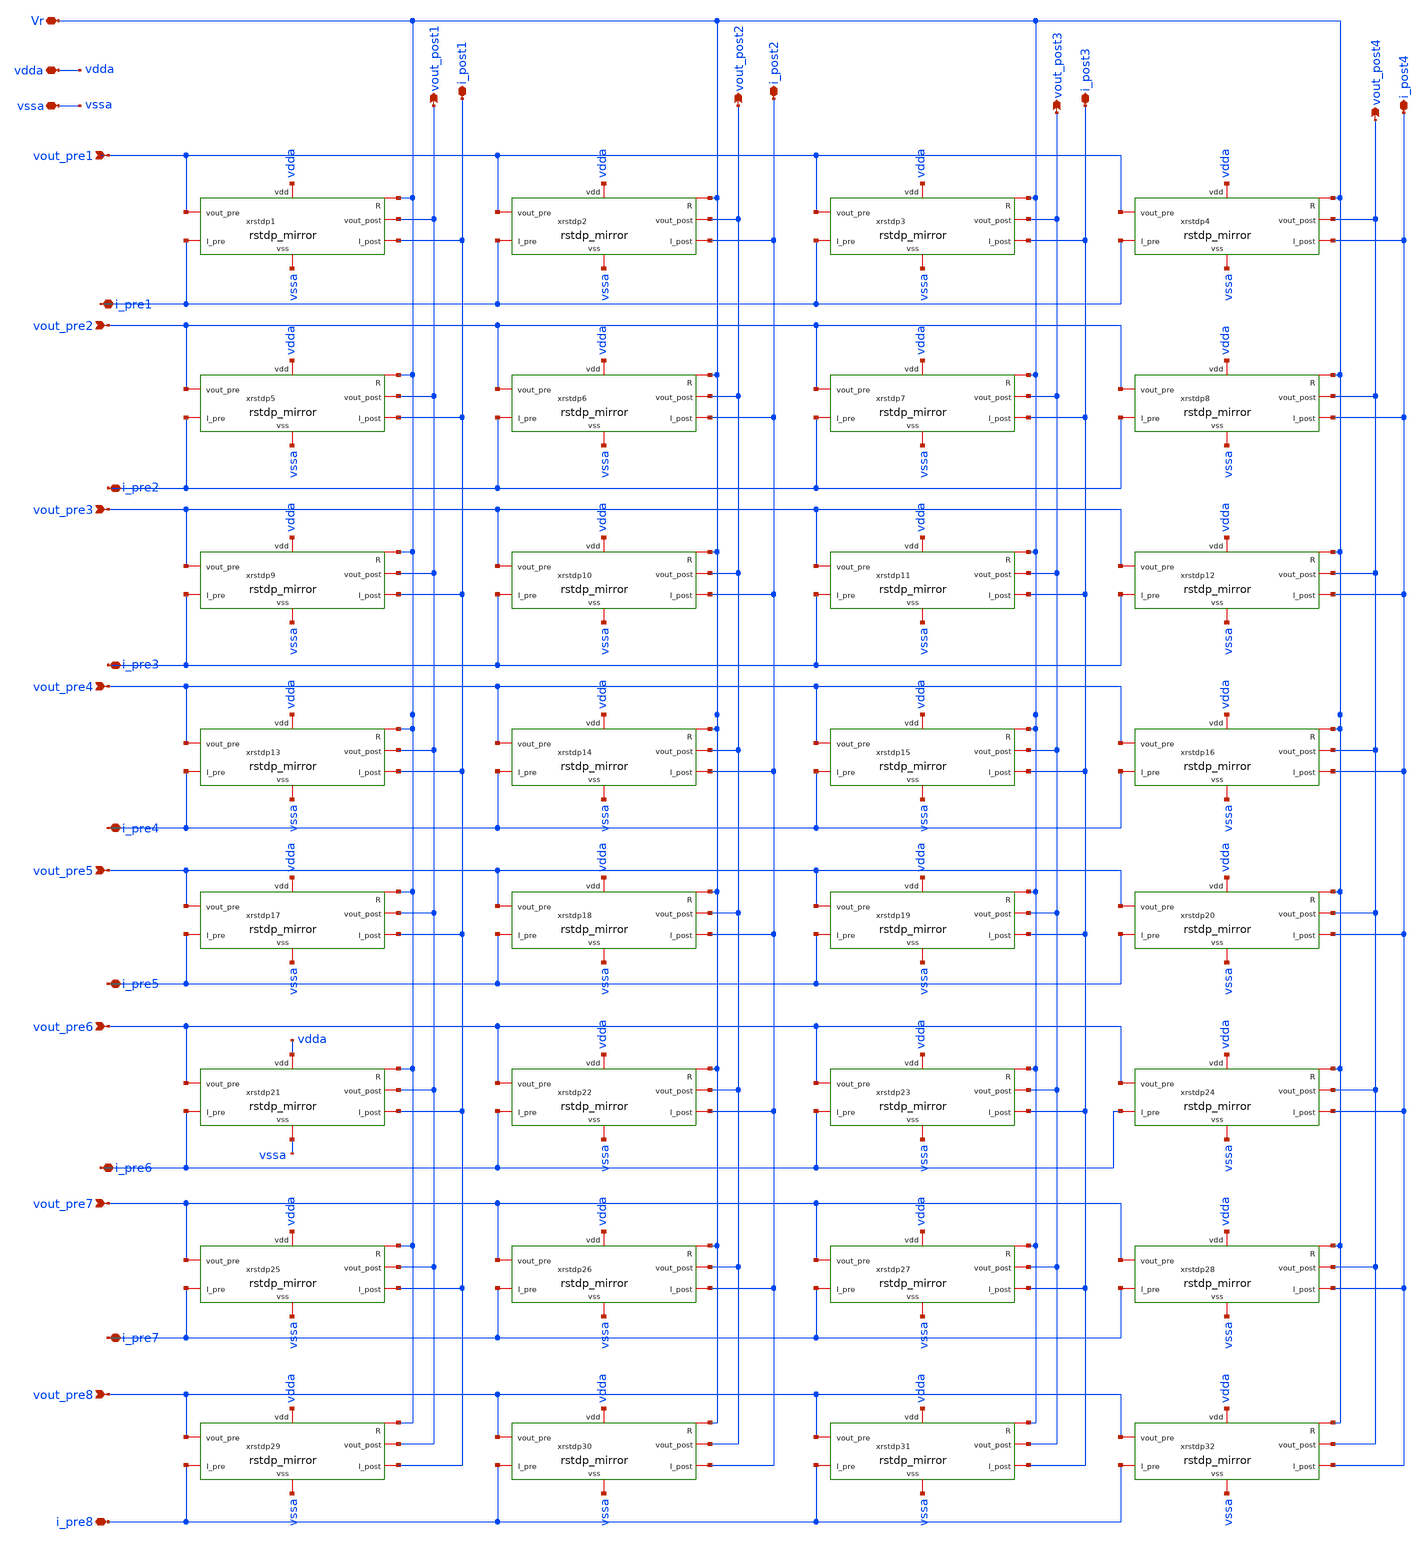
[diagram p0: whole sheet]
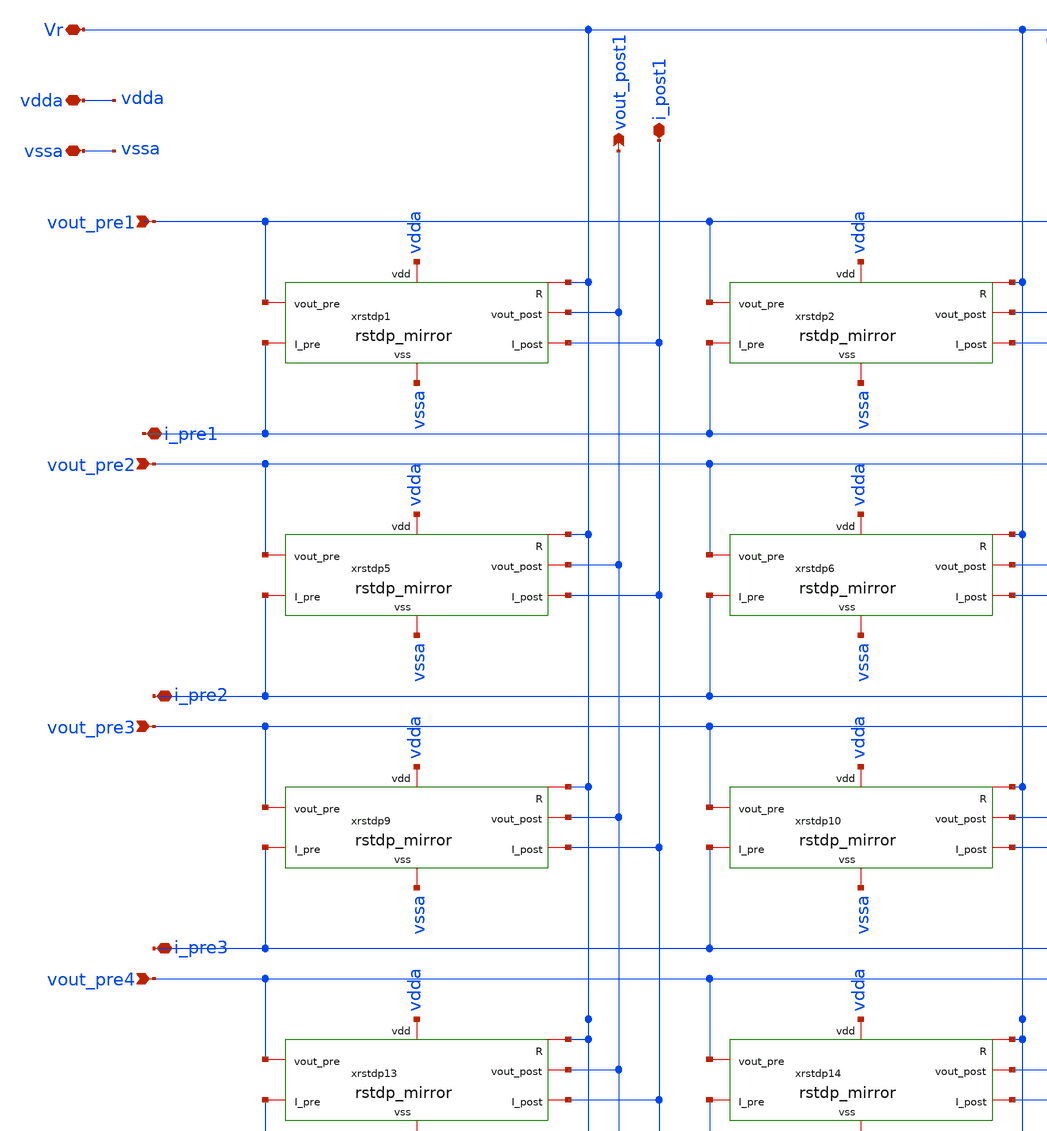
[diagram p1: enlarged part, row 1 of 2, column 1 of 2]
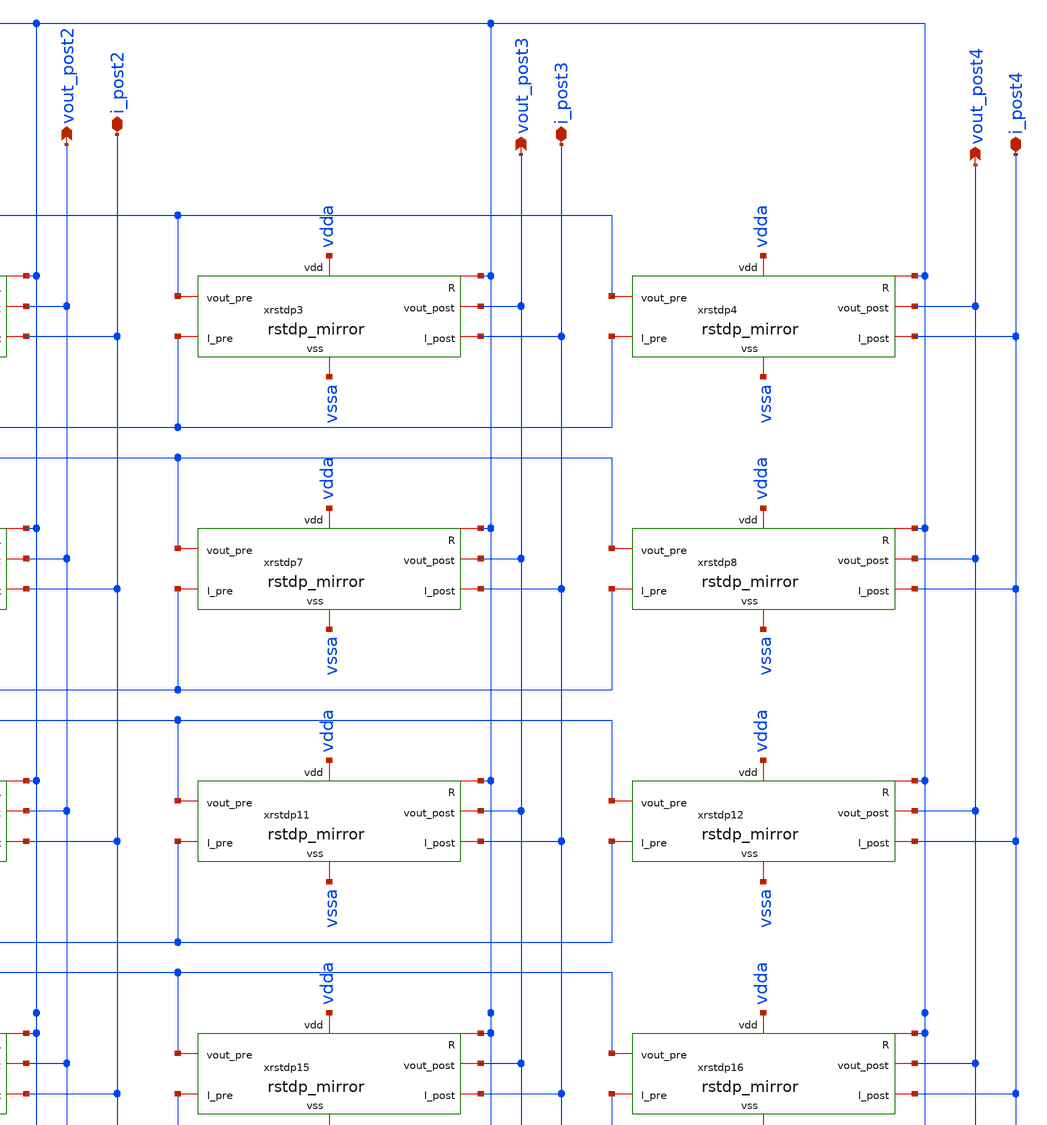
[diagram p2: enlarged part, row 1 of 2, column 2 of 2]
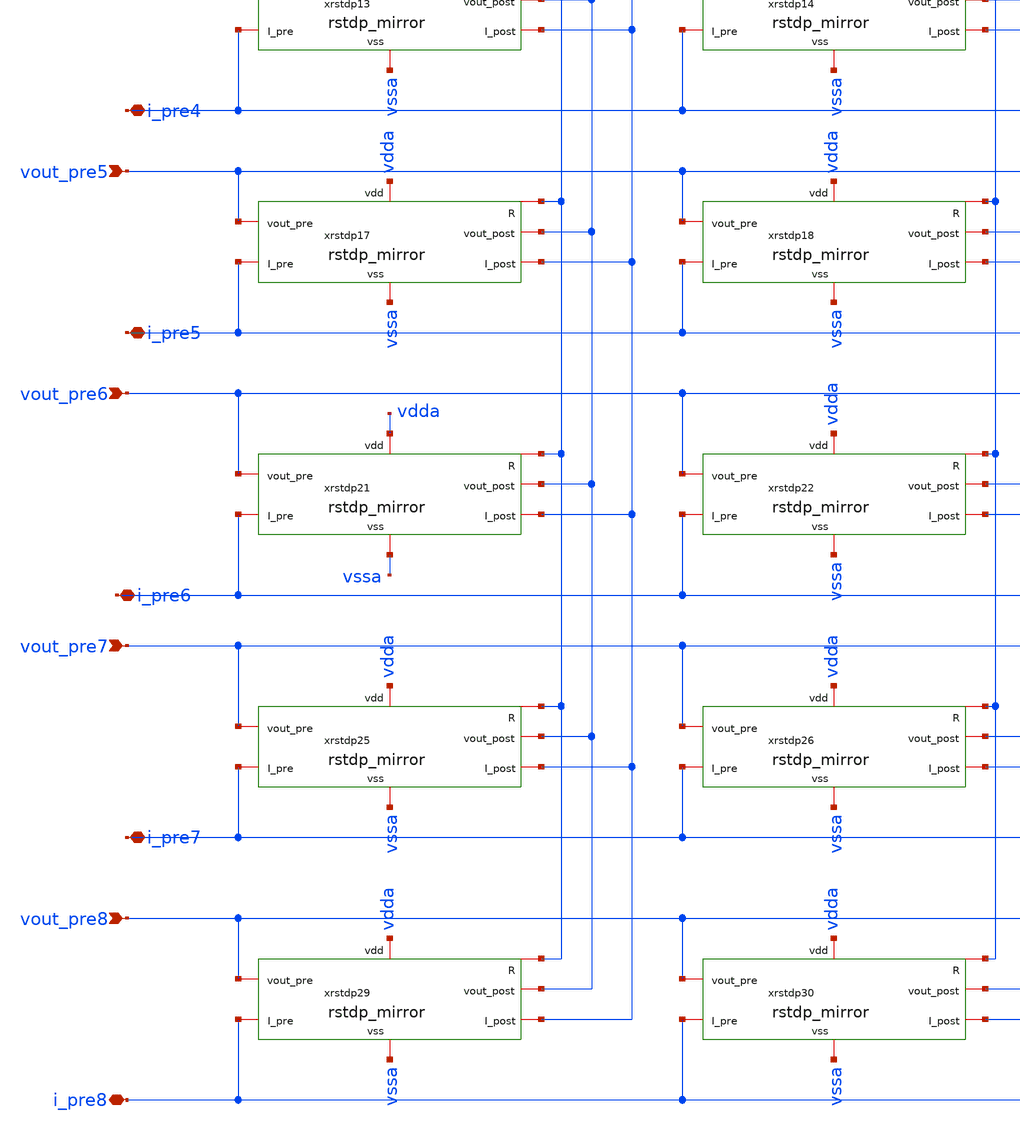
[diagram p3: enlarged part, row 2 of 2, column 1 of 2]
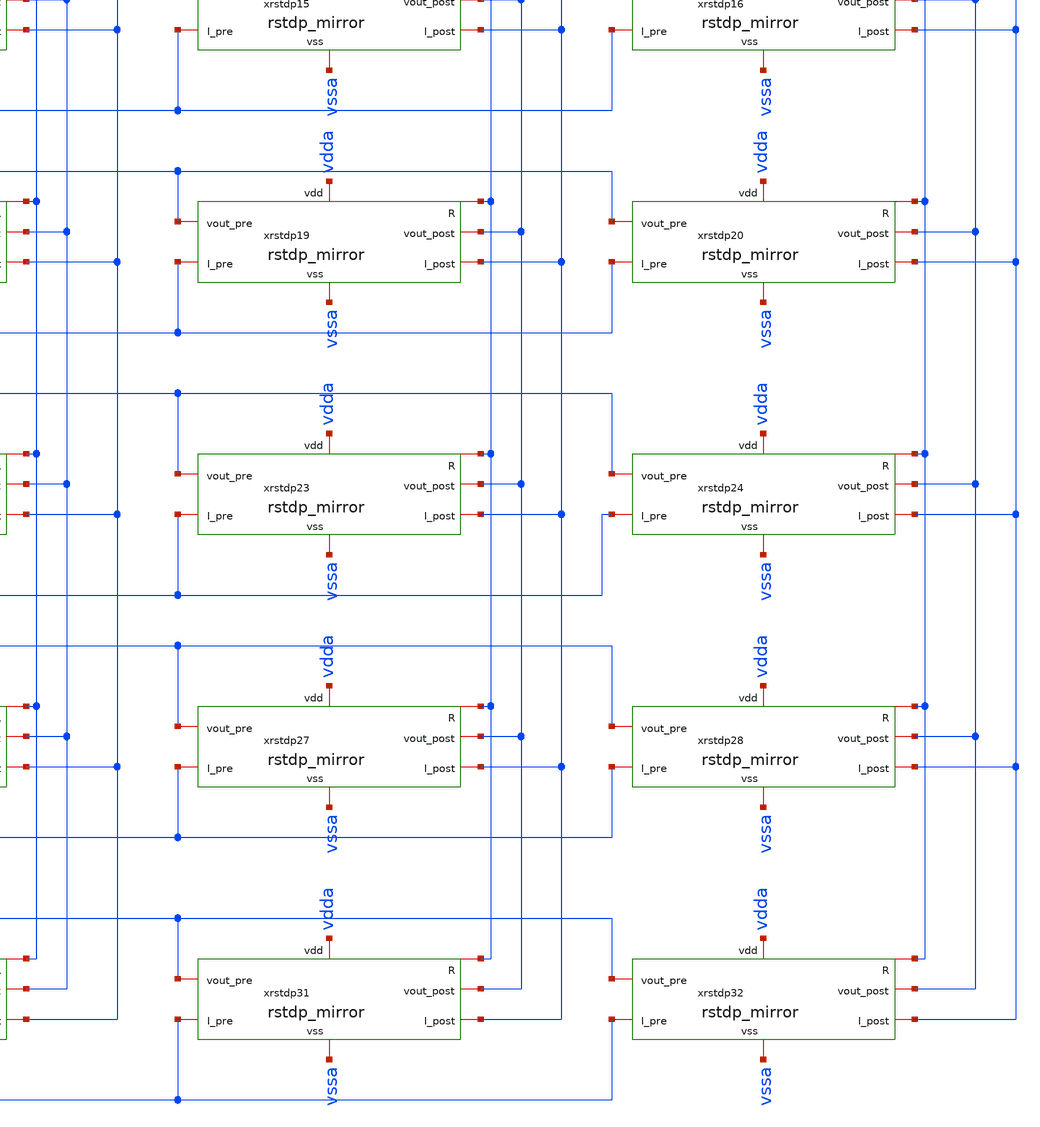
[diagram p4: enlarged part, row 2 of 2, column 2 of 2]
** sch_path: Synapse/rstdp_array_8x4.sch
**.subckt rstdp_array_8x4 vout_pre1 vout_post1 i_pre1 vdda vssa i_post1 i_post3 i_post4 i_pre2
*+ i_pre3 i_pre4 vout_pre2 vout_pre3 vout_pre4 vout_post2 vout_post3 vout_post4 i_post2 Vr i_pre5 i_pre6
*+ i_pre7 i_pre8 vout_pre5 vout_pre6 vout_pre7 vout_pre8
*.ipin vout_pre1
*.opin vout_post1
*.iopin i_pre1
*.iopin vdda
*.iopin vssa
*.iopin i_post1
*.iopin i_post3
*.iopin i_post4
*.iopin i_pre2
*.iopin i_pre3
*.iopin i_pre4
*.ipin vout_pre2
*.ipin vout_pre3
*.ipin vout_pre4
*.opin vout_post2
*.opin vout_post3
*.opin vout_post4
*.iopin i_post2
*.iopin Vr
*.iopin i_pre5
*.iopin i_pre6
*.iopin i_pre7
*.iopin i_pre8
*.ipin vout_pre5
*.ipin vout_pre6
*.ipin vout_pre7
*.ipin vout_pre8
xrstdp1 vdda Vr vssa vout_pre1 vout_post1 i_post1 i_pre1 rstdp_mirror
xrstdp2 vdda Vr vssa vout_pre1 vout_post2 i_post2 i_pre1 rstdp_mirror
xrstdp3 vdda Vr vssa vout_pre1 vout_post3 i_post3 i_pre1 rstdp_mirror
xrstdp4 vdda Vr vssa vout_pre1 vout_post4 i_post4 i_pre1 rstdp_mirror
xrstdp5 vdda Vr vssa vout_pre2 vout_post1 i_post1 i_pre2 rstdp_mirror
xrstdp6 vdda Vr vssa vout_pre2 vout_post2 i_post2 i_pre2 rstdp_mirror
xrstdp7 vdda Vr vssa vout_pre2 vout_post3 i_post3 i_pre2 rstdp_mirror
xrstdp8 vdda Vr vssa vout_pre2 vout_post4 i_post4 i_pre2 rstdp_mirror
xrstdp9 vdda Vr vssa vout_pre3 vout_post1 i_post1 i_pre3 rstdp_mirror
xrstdp10 vdda Vr vssa vout_pre3 vout_post2 i_post2 i_pre3 rstdp_mirror
xrstdp11 vdda Vr vssa vout_pre3 vout_post3 i_post3 i_pre3 rstdp_mirror
xrstdp12 vdda Vr vssa vout_pre3 vout_post4 i_post4 i_pre3 rstdp_mirror
xrstdp13 vdda Vr vssa vout_pre4 vout_post1 i_post1 i_pre4 rstdp_mirror
xrstdp14 vdda Vr vssa vout_pre4 vout_post2 i_post2 i_pre4 rstdp_mirror
xrstdp15 vdda Vr vssa vout_pre4 vout_post3 i_post3 i_pre4 rstdp_mirror
xrstdp16 vdda Vr vssa vout_pre4 vout_post4 i_post4 i_pre4 rstdp_mirror
xrstdp17 vdda Vr vssa vout_pre5 vout_post1 i_post1 i_pre5 rstdp_mirror
xrstdp18 vdda Vr vssa vout_pre5 vout_post2 i_post2 i_pre5 rstdp_mirror
xrstdp19 vdda Vr vssa vout_pre5 vout_post3 i_post3 i_pre5 rstdp_mirror
xrstdp20 vdda Vr vssa vout_pre5 vout_post4 i_post4 i_pre5 rstdp_mirror
xrstdp21 vdda Vr vssa vout_pre6 vout_post1 i_post1 i_pre6 rstdp_mirror
xrstdp22 vdda Vr vssa vout_pre6 vout_post2 i_post2 i_pre6 rstdp_mirror
xrstdp23 vdda Vr vssa vout_pre6 vout_post3 i_post3 i_pre6 rstdp_mirror
xrstdp24 vdda Vr vssa vout_pre6 vout_post4 i_post4 i_pre6 rstdp_mirror
xrstdp25 vdda Vr vssa vout_pre7 vout_post1 i_post1 i_pre7 rstdp_mirror
xrstdp26 vdda Vr vssa vout_pre7 vout_post2 i_post2 i_pre7 rstdp_mirror
xrstdp27 vdda Vr vssa vout_pre7 vout_post3 i_post3 i_pre7 rstdp_mirror
xrstdp28 vdda Vr vssa vout_pre7 vout_post4 i_post4 i_pre7 rstdp_mirror
xrstdp29 vdda Vr vssa vout_pre8 vout_post1 i_post1 i_pre8 rstdp_mirror
xrstdp30 vdda Vr vssa vout_pre8 vout_post2 i_post2 i_pre8 rstdp_mirror
xrstdp31 vdda Vr vssa vout_pre8 vout_post3 i_post3 i_pre8 rstdp_mirror
xrstdp32 vdda Vr vssa vout_pre8 vout_post4 i_post4 i_pre8 rstdp_mirror
**.ends

* expanding   symbol:  Synapse/rstdp_mirror.sym # of pins=7
** sym_path: Synapse/rstdp_mirror.sym
** sch_path: Synapse/rstdp_mirror.sch
.subckt rstdp_mirror vdd R vss vout_pre vout_post I_post I_pre
*.iopin vdd
*.iopin vss
*.iopin R
*.iopin vout_post
*.iopin vout_pre
*.iopin I_post
*.iopin I_pre
XM2 A vout_pre vpre vss sky130_fd_pr__nfet_01v8 L=0.15 W=1.5 nf=1 ad='int((nf+1)/2) * W/nf * 0.29' as='int((nf+2)/2) * W/nf * 0.29'
+ pd='2*int((nf+1)/2) * (W/nf + 0.29)' ps='2*int((nf+2)/2) * (W/nf + 0.29)' nrd='0.29 / W' nrs='0.29 / W'
+ sa=0 sb=0 sd=0 mult=1 m=1
XM3 vpre vout_post vss vss sky130_fd_pr__nfet_01v8 L=0.15 W=1.5 nf=1 ad='int((nf+1)/2) * W/nf * 0.29'
+ as='int((nf+2)/2) * W/nf * 0.29' pd='2*int((nf+1)/2) * (W/nf + 0.29)' ps='2*int((nf+2)/2) * (W/nf + 0.29)'
+ nrd='0.29 / W' nrs='0.29 / W' sa=0 sb=0 sd=0 mult=1 m=1
XM1 A vout_post vpost vss sky130_fd_pr__nfet_01v8 L=0.15 W=1.5 nf=1 ad='int((nf+1)/2) * W/nf * 0.29'
+ as='int((nf+2)/2) * W/nf * 0.29' pd='2*int((nf+1)/2) * (W/nf + 0.29)' ps='2*int((nf+2)/2) * (W/nf + 0.29)'
+ nrd='0.29 / W' nrs='0.29 / W' sa=0 sb=0 sd=0 mult=1 m=1
XM4 vpost vout_pre vss vss sky130_fd_pr__nfet_01v8 L=0.15 W=1.5 nf=1 ad='int((nf+1)/2) * W/nf * 0.29'
+ as='int((nf+2)/2) * W/nf * 0.29' pd='2*int((nf+1)/2) * (W/nf + 0.29)' ps='2*int((nf+2)/2) * (W/nf + 0.29)'
+ nrd='0.29 / W' nrs='0.29 / W' sa=0 sb=0 sd=0 mult=1 m=1
XM10 vss A vdd vdd sky130_fd_pr__pfet_01v8 L=5 W=0.5 nf=1 ad='int((nf+1)/2) * W/nf * 0.29' as='int((nf+2)/2) * W/nf * 0.29'
+ pd='2*int((nf+1)/2) * (W/nf + 0.29)' ps='2*int((nf+2)/2) * (W/nf + 0.29)' nrd='0.29 / W' nrs='0.29 / W'
+ sa=0 sb=0 sd=0 mult=1 m=1
XR2 te be rram_v0
XM5 vpre R be vss sky130_fd_pr__nfet_01v8 L=0.15 W=1.5 nf=1 ad='int((nf+1)/2) * W/nf * 0.29' as='int((nf+2)/2) * W/nf * 0.29'
+ pd='2*int((nf+1)/2) * (W/nf + 0.29)' ps='2*int((nf+2)/2) * (W/nf + 0.29)' nrd='0.29 / W' nrs='0.29 / W'
+ sa=0 sb=0 sd=0 mult=1 m=1
XM6 te R vpost vss sky130_fd_pr__nfet_01v8 L=0.15 W=1.5 nf=1 ad='int((nf+1)/2) * W/nf * 0.29' as='int((nf+2)/2) * W/nf * 0.29'
+ pd='2*int((nf+1)/2) * (W/nf + 0.29)' ps='2*int((nf+2)/2) * (W/nf + 0.29)' nrd='0.29 / W' nrs='0.29 / W'
+ sa=0 sb=0 sd=0 mult=1 m=1
XM7 vpre R te vdd sky130_fd_pr__pfet_01v8 L=0.15 W=3 nf=1 ad='int((nf+1)/2) * W/nf * 0.29' as='int((nf+2)/2) * W/nf * 0.29'
+ pd='2*int((nf+1)/2) * (W/nf + 0.29)' ps='2*int((nf+2)/2) * (W/nf + 0.29)' nrd='0.29 / W' nrs='0.29 / W'
+ sa=0 sb=0 sd=0 mult=1 m=1
XM8 be R vpost vdd sky130_fd_pr__pfet_01v8 L=0.15 W=3 nf=1 ad='int((nf+1)/2) * W/nf * 0.29' as='int((nf+2)/2) * W/nf * 0.29'
+ pd='2*int((nf+1)/2) * (W/nf + 0.29)' ps='2*int((nf+2)/2) * (W/nf + 0.29)' nrd='0.29 / W' nrs='0.29 / W'
+ sa=0 sb=0 sd=0 mult=1 m=1
XM14 I_post A vdd vdd sky130_fd_pr__pfet_01v8 L=0.4 W=1 nf=1 ad='int((nf+1)/2) * W/nf * 0.29' as='int((nf+2)/2) * W/nf * 0.29'
+ pd='2*int((nf+1)/2) * (W/nf + 0.29)' ps='2*int((nf+2)/2) * (W/nf + 0.29)' nrd='0.29 / W' nrs='0.29 / W'
+ sa=0 sb=0 sd=0 mult=1 m=1
XM15 A A vdd vdd sky130_fd_pr__pfet_01v8 L=0.15 W=2.5 nf=1 ad='int((nf+1)/2) * W/nf * 0.29' as='int((nf+2)/2) * W/nf * 0.29'
+ pd='2*int((nf+1)/2) * (W/nf + 0.29)' ps='2*int((nf+2)/2) * (W/nf + 0.29)' nrd='0.29 / W' nrs='0.29 / W'
+ sa=0 sb=0 sd=0 mult=1 m=1
* noconn I_pre
.ends

.end
